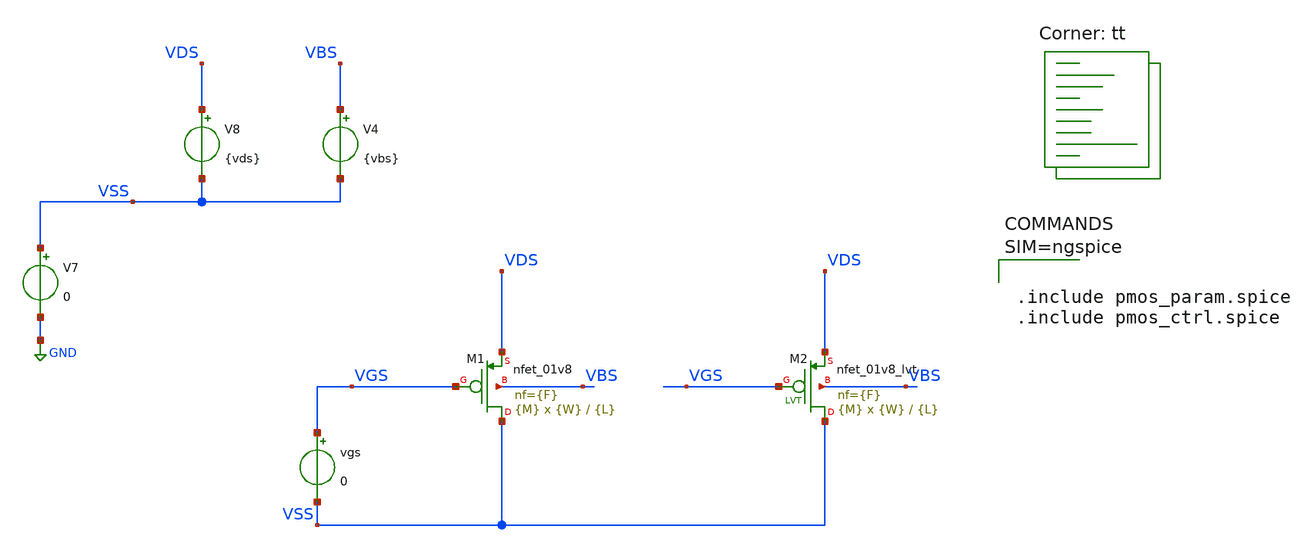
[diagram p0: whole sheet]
** sch_path: work/design/pmos.sch
**.subckt pmos
XM1 VSS VGS VDS VBS sky130_fd_pr__nfet_01v8 L={L} W={W} nf={F} ad='int((nf+1)/2) * W/nf * 0.29' as='int((nf+2)/2) * W/nf * 0.29'
+ pd='2*int((nf+1)/2) * (W/nf + 0.29)' ps='2*int((nf+2)/2) * (W/nf + 0.29)' nrd='0.29 / W' nrs='0.29 / W'
+ sa=0 sb=0 sd=0 mult={M} m={M}
vgs VGS VSS 0
V4 VBS VSS {vbs}
V7 VSS GND 0
V8 VDS VSS {vds}
XM2 VSS VGS VDS VBS sky130_fd_pr__nfet_01v8_lvt L={L} W={W} nf={F} ad='int((nf+1)/2) * W/nf * 0.29' as='int((nf+2)/2) * W/nf * 0.29'
+ pd='2*int((nf+1)/2) * (W/nf + 0.29)' ps='2*int((nf+2)/2) * (W/nf + 0.29)' nrd='0.29 / W' nrs='0.29 / W'
+ sa=0 sb=0 sd=0 mult={M} m={M}
**** begin user architecture code
.lib $::SKYWATER_MODELS/sky130.lib.spice tt



.include pmos_param.spice
.include pmos_ctrl.spice



**** end user architecture code
**.ends
.GLOBAL GND
.end
